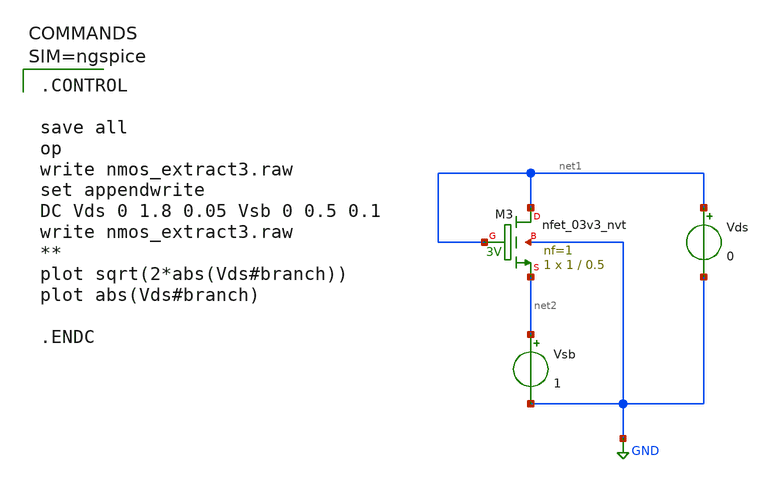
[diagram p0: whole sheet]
** sch_path: work/xschem/nmos_extract3.sch
**.subckt nmos_extract3
Vsb net2 GND 1
Vds net1 GND 0
XM3 net1 net1 net2 GND sky130_fd_pr__nfet_03v3_nvt L=0.5 W=1 nf=1 ad='int((1 + 1)/2) * 1 / 1 * 0.29'
+ as='int((1 + 2)/2) * 1 / 1 * 0.29' pd='2*int((1 + 1)/2) * (1 / 1 + 0.29)' ps='2*int((1 + 2)/2) * (1 / 1 + 0.29)'
+ nrd='0.29 / 1 ' nrs='0.29 / 1 ' sa=0 sb=0 sd=0 mult=1 m=1
**** begin user architecture code


.CONTROL

save all
op
write nmos_extract3.raw
set appendwrite
DC Vds 0 1.8 0.05 Vsb 0 0.5 0.1
write nmos_extract3.raw
**
plot sqrt(2*abs(Vds#branch))
plot abs(Vds#branch)

.ENDC




** opencircuitdesign pdks install
.lib $::SKYWATER_MODELS/sky130.lib.spice tt

**** end user architecture code
**.ends
.GLOBAL GND
.end
